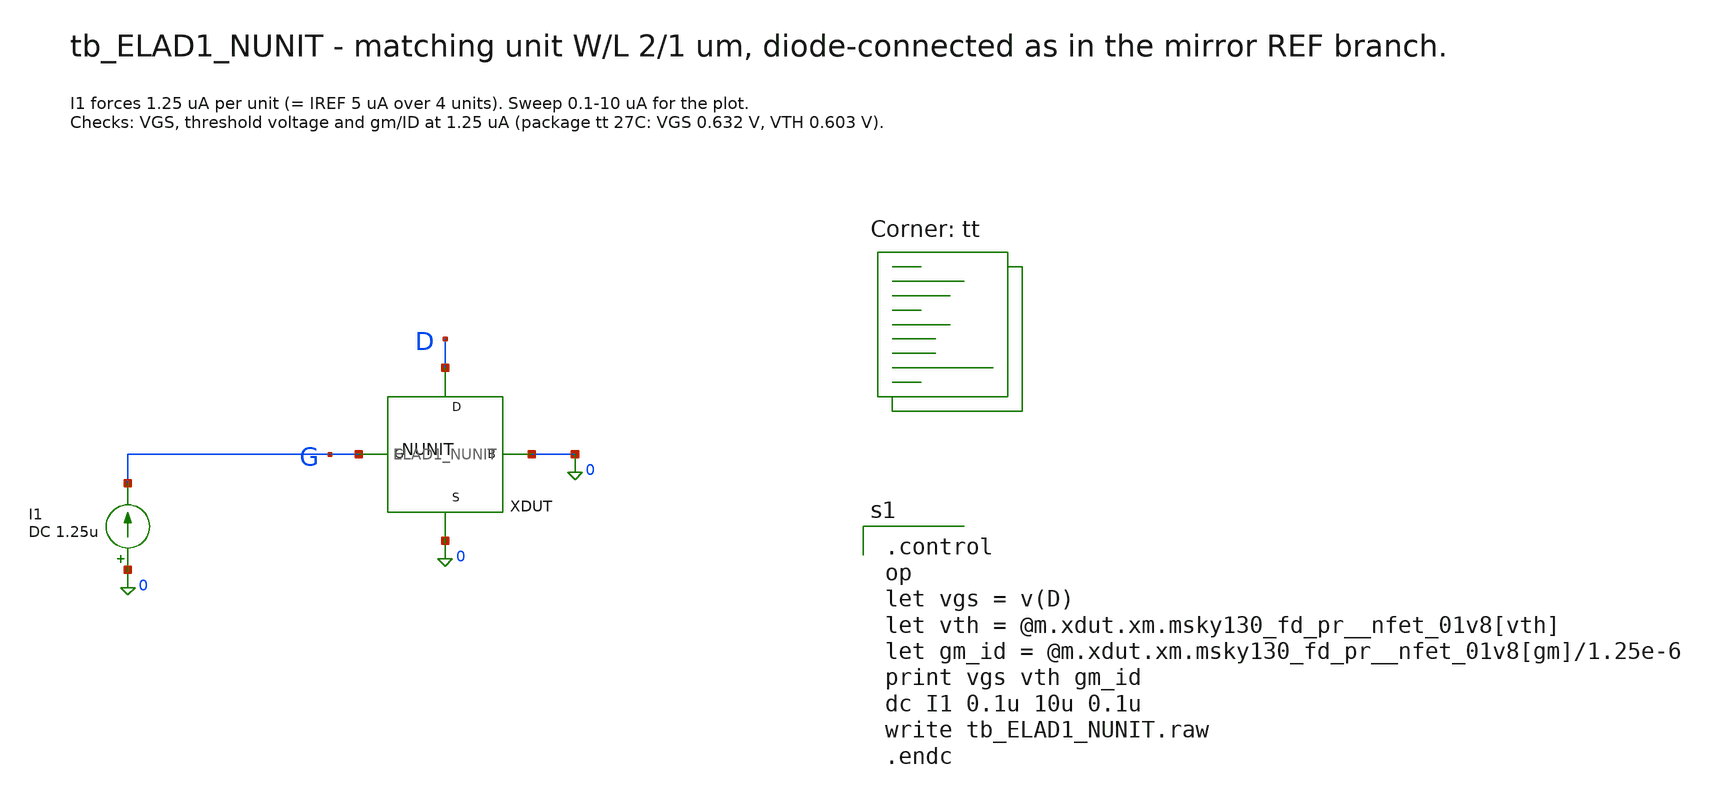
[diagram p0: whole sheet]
** sch_path: cells/ELAD1_NUNIT/schematic/tb_ELAD1_NUNIT.sch
**.subckt tb_ELAD1_NUNIT
XDUT D G 0 0 ELAD1_NUNIT
I1 0 G DC 1.25u
**** begin user architecture code

.control
op
let vgs = v(D)
let vth = @m.xdut.xm.msky130_fd_pr__nfet_01v8[vth]
let gm_id = @m.xdut.xm.msky130_fd_pr__nfet_01v8[gm]/1.25e-6
print vgs vth gm_id
dc I1 0.1u 10u 0.1u
write tb_ELAD1_NUNIT.raw
.endc

.lib $::SKYWATER_MODELS/sky130.lib.spice tt
**** end user architecture code
**.ends

* expanding   symbol:  ELAD1_NUNIT.sym # of pins=4
** sym_path: cells/ELAD1_NUNIT/schematic/ELAD1_NUNIT.sym
** sch_path: cells/ELAD1_NUNIT/schematic/ELAD1_NUNIT.sch
.subckt ELAD1_NUNIT D G S B
*.iopin D
*.iopin G
*.iopin S
*.iopin B
XM D G S B sky130_fd_pr__nfet_01v8 L=1 W=2 nf=1 ad='int((1 + 1)/2) * 2 / 1 * 0.29' as='int((1 + 2)/2) * 2 / 1 * 0.29'
+ pd='2*int((1 + 1)/2) * (2 / 1 + 0.29)' ps='2*int((1 + 2)/2) * (2 / 1 + 0.29)' nrd='0.29 / 2 ' nrs='0.29 / 2 '
+ sa=0 sb=0 sd=0 mult=1 m=1
.ends

.end
